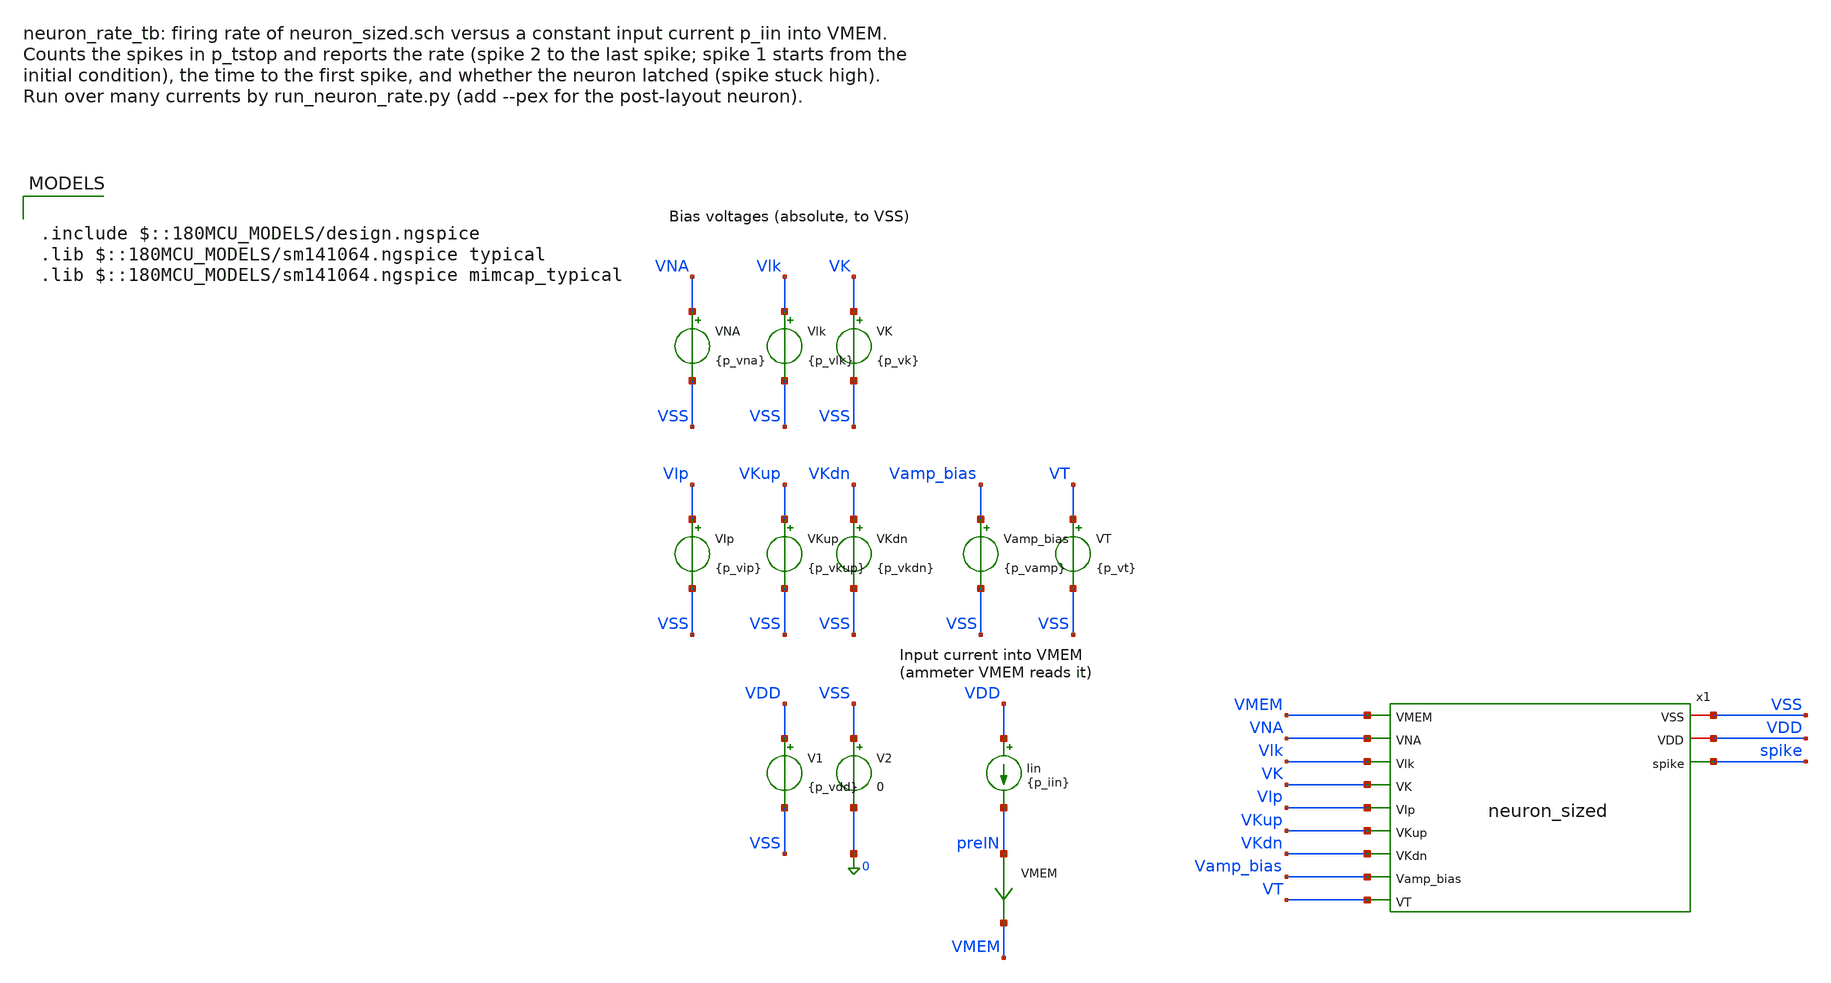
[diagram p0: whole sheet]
** sch_path: analog/testbenches/neuron/neuron_rate_tb.sch
**.subckt neuron_rate_tb
V1 VDD VSS {p_vdd}
V2 VSS 0 0
Iin VDD preIN {p_iin}
VMEM preIN VMEM 0
.save i(vmem)
x1 VSS VDD VMEM VNA Vlk VK VIp VKup VKdn Vamp_bias VT spike neuron_sized
Vlk Vlk VSS {p_vlk}
VK VK VSS {p_vk}
VNA VNA VSS {p_vna}
VKup VKup VSS {p_vkup}
VKdn VKdn VSS {p_vkdn}
VIp VIp VSS {p_vip}
VT VT VSS {p_vt}
Vamp_bias Vamp_bias VSS {p_vamp}
**** begin user architecture code

.include $::180MCU_MODELS/design.ngspice
.lib $::180MCU_MODELS/sm141064.ngspice typical
.lib $::180MCU_MODELS/sm141064.ngspice mimcap_typical



* Biases of neuron_sized (as in neuron_nominal_tb). p_iin, p_tstop and p_tmax
* (maximum time step) are set per point by run_neuron_rate.py.
.param p_vdd=3.3 p_iin=9.5n p_tstop=2m p_tmax=100n
.param p_vlk=0.425 p_vamp=0.535 p_vip=0.573 p_vna=1.93 p_vkup=2.35 p_vk=1.22 p_vkdn=0.588 p_vt=1.66
.csparam vdd_c={p_vdd}
.csparam tstop_c={p_tstop}
.csparam tmax_c={p_tmax}
.csparam iin_c={p_iin}
.ic v(VMEM)=0 v(spike)=0
.control
  save v(spike) v(VMEM)
  tran 20n $&tstop_c 0 $&tmax_c uic
  let vsw = vdd_c/2

  * Count rising edges of spike through VDD/2 (a failed meas keeps -1)
  let n = 0
  let k = 1
  let t1 = -1
  let t2 = -1
  let tlast = -1
  while k <= 2000
    let tk = -1
    meas tran tk when v(spike)=$&vsw rise=$&k
    if tk < 0
      break
    end
    if k = 1
      let t1 = tk
    end
    if k = 2
      let t2 = tk
    end
    let tlast = tk
    let n = k
    let k = k + 1
  end

  * rate: from spike 2 to the last spike (spike 1 starts from VMEM = 0)
  let rate = 0
  if n >= 3
    let rate = (n - 2)/(tlast - t2)
  end
  * Latch check over the last 20 % of the run: spike stuck high, VMEM range
  let tw = 0.8*tstop_c
  meas tran spike_min_end min v(spike) from=$&tw to=$&tstop_c
  meas tran spike_max_end max v(spike) from=$&tw to=$&tstop_c
  meas tran vmem_max_end max v(VMEM) from=$&tw to=$&tstop_c
  meas tran vmem_min_end min v(VMEM) from=$&tw to=$&tstop_c
  meas tran spike_max max v(spike)

  echo RES iin=$&iin_c
  echo RES nspikes=$&n
  echo RES rate=$&rate
  echo RES t_first=$&t1
  echo RES t_last=$&tlast
  echo RES spike_max=$&spike_max
  echo RES spike_min_end=$&spike_min_end
  echo RES spike_max_end=$&spike_max_end
  echo RES vmem_max_end=$&vmem_max_end
  echo RES vmem_min_end=$&vmem_min_end
  echo neuron_rate_tb: iin $&iin_c A, $&n spikes in $&tstop_c s, rate $&rate Hz

  set wr_singlescale
  set wr_vecnames
  if $?batchmode = 0
    wrdata /foss/designs/engn2912e-project/analog/testbenches/neuron/results/neuron_rate_tb.txt
+ v(VMEM) v(spike)
    plot v(VMEM) v(spike) title 'neuron_rate_tb: membrane and spike' xlabel 't (s)' ylabel 'V'
  else
    wrdata neuron_rate_tb.txt v(VMEM) v(spike)
  end
.endc


**** end user architecture code
**.ends
.end
